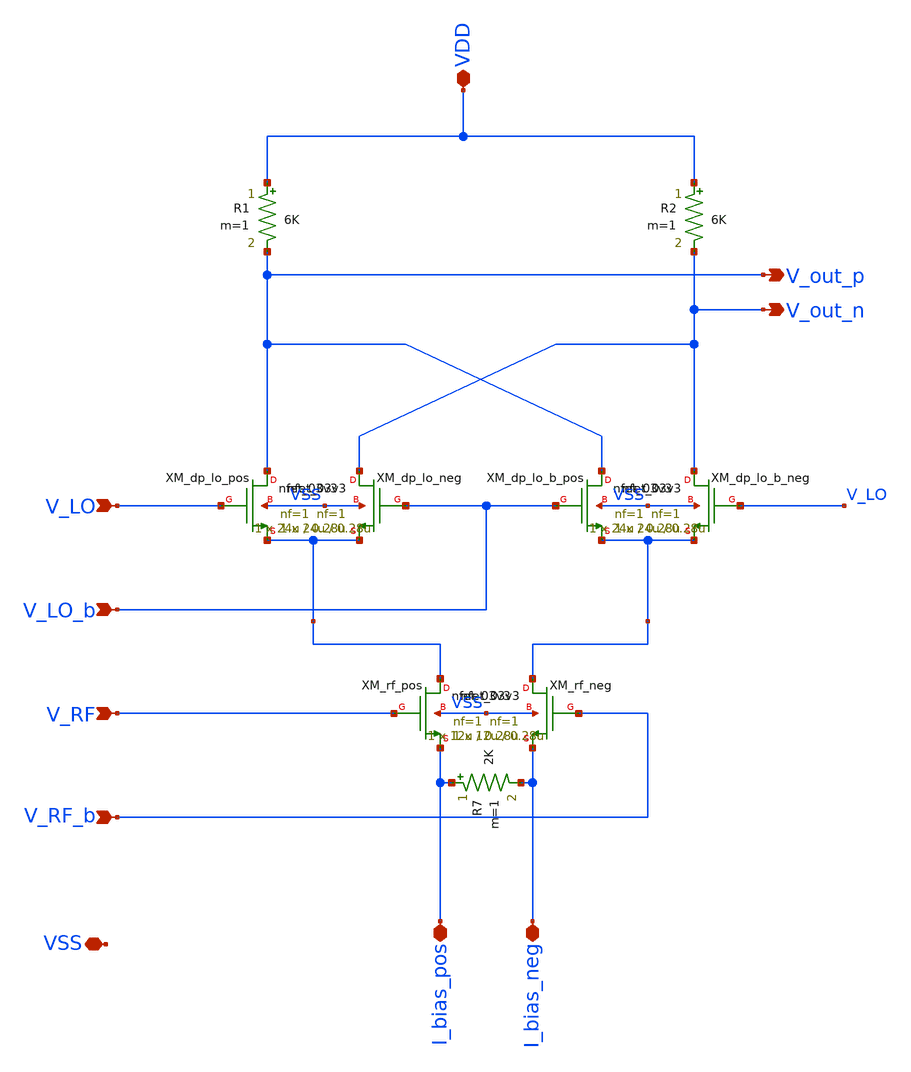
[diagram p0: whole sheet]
** sch_path: src/design_xsch/Gilbert_cell_no_hierarchy.sch
**.subckt Gilbert_cell_no_hierarchy V_LO V_LO_b V_RF V_RF_b V_out_p V_out_n I_bias_neg I_bias_pos
*+ VDD VSS
*.ipin V_LO
*.ipin V_LO_b
*.ipin V_RF
*.ipin V_RF_b
*.opin V_out_p
*.opin V_out_n
*.iopin I_bias_neg
*.iopin I_bias_pos
*.iopin VDD
*.iopin VSS
R1 VDD V_out_p 6K m=1
R2 VDD V_out_n 6K m=1
XM_dp_lo_pos V_out_p V_LO rf_diff_pair_pos_input VSS nfet_03v3 L=0.28u W=24u nf=1 ad='int((nf+1)/2) * W/nf * 0.18u'
+ as='int((nf+2)/2) * W/nf * 0.18u' pd='2*int((nf+1)/2) * (W/nf + 0.18u)' ps='2*int((nf+2)/2) * (W/nf + 0.18u)'
+ nrd='0.18u / W' nrs='0.18u / W' sa=0 sb=0 sd=0 m=1
XM_dp_lo_neg V_out_n V_LO_b rf_diff_pair_pos_input VSS nfet_03v3 L=0.28u W=24u nf=1 ad='int((nf+1)/2) * W/nf * 0.18u'
+ as='int((nf+2)/2) * W/nf * 0.18u' pd='2*int((nf+1)/2) * (W/nf + 0.18u)' ps='2*int((nf+2)/2) * (W/nf + 0.18u)'
+ nrd='0.18u / W' nrs='0.18u / W' sa=0 sb=0 sd=0 m=1
XM_dp_lo_b_pos V_out_p V_LO_b rf_diff_pair_neg_input VSS nfet_03v3 L=0.28u W=24u nf=1 ad='int((nf+1)/2) * W/nf * 0.18u'
+ as='int((nf+2)/2) * W/nf * 0.18u' pd='2*int((nf+1)/2) * (W/nf + 0.18u)' ps='2*int((nf+2)/2) * (W/nf + 0.18u)'
+ nrd='0.18u / W' nrs='0.18u / W' sa=0 sb=0 sd=0 m=1
XM_dp_lo_b_neg V_out_n V_LO rf_diff_pair_neg_input VSS nfet_03v3 L=0.28u W=24u nf=1 ad='int((nf+1)/2) * W/nf * 0.18u'
+ as='int((nf+2)/2) * W/nf * 0.18u' pd='2*int((nf+1)/2) * (W/nf + 0.18u)' ps='2*int((nf+2)/2) * (W/nf + 0.18u)'
+ nrd='0.18u / W' nrs='0.18u / W' sa=0 sb=0 sd=0 m=1
XM_rf_pos rf_diff_pair_pos_input V_RF I_bias_pos VSS nfet_03v3 L=0.28u W=12u nf=1 ad='int((nf+1)/2) * W/nf * 0.18u'
+ as='int((nf+2)/2) * W/nf * 0.18u' pd='2*int((nf+1)/2) * (W/nf + 0.18u)' ps='2*int((nf+2)/2) * (W/nf + 0.18u)'
+ nrd='0.18u / W' nrs='0.18u / W' sa=0 sb=0 sd=0 m=1
XM_rf_neg rf_diff_pair_neg_input V_RF_b I_bias_neg VSS nfet_03v3 L=0.28u W=12u nf=1 ad='int((nf+1)/2) * W/nf * 0.18u'
+ as='int((nf+2)/2) * W/nf * 0.18u' pd='2*int((nf+1)/2) * (W/nf + 0.18u)' ps='2*int((nf+2)/2) * (W/nf + 0.18u)'
+ nrd='0.18u / W' nrs='0.18u / W' sa=0 sb=0 sd=0 m=1
R7 I_bias_pos I_bias_neg 2K m=1
**.ends
.end
